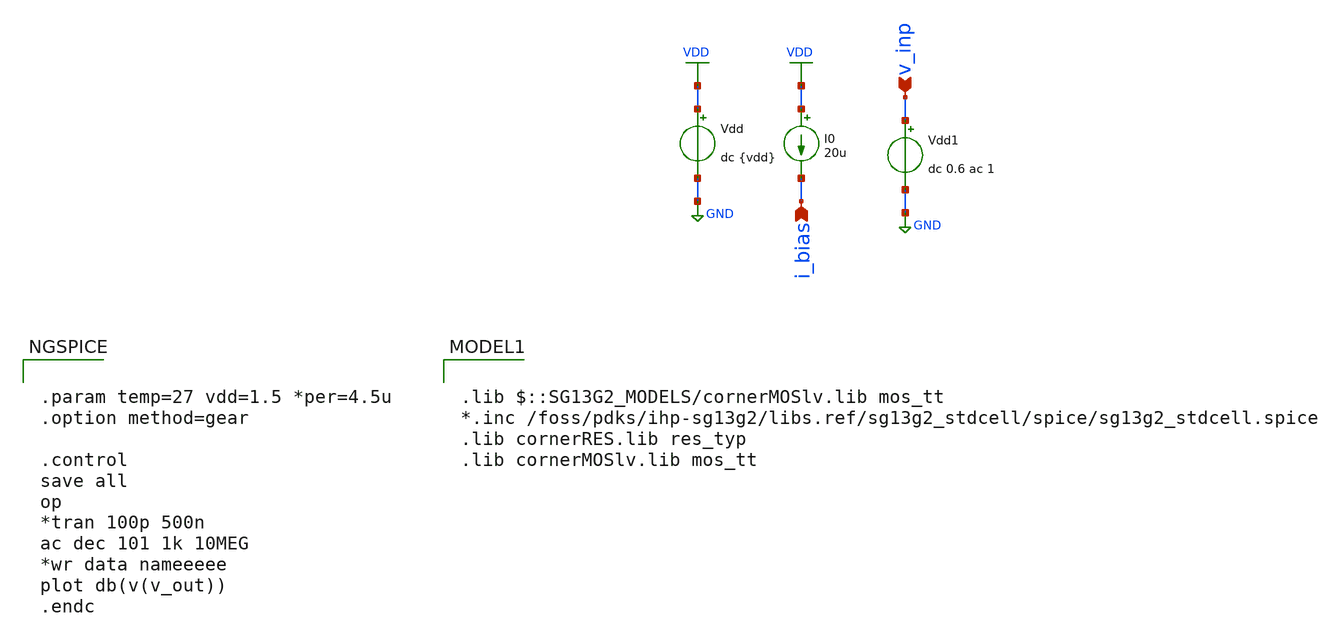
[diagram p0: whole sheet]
** sch_path: 3_Real_Cir/20_Real_Cir/tb_ota.sch
**.subckt tb_ota i_bias v_inp
*.ipin i_bias
*.ipin v_inp
Vdd VDD GND dc {vdd}
I0 VDD i_bias 20u
Vdd1 v_inp GND dc 0.6 ac 1
**** begin user architecture code

.lib $::SG13G2_MODELS/cornerMOSlv.lib mos_tt
*.inc /foss/pdks/ihp-sg13g2/libs.ref/sg13g2_stdcell/spice/sg13g2_stdcell.spice
.lib cornerRES.lib res_typ
.lib cornerMOSlv.lib mos_tt



.param temp=27 vdd=1.5 *per=4.5u
.option method=gear

.control
save all
op
*tran 100p 500n
ac dec 101 1k 10MEG
*wr data nameeeee
plot db(v(v_out))
.endc


**** end user architecture code
**.ends
.GLOBAL GND
.GLOBAL VDD
.end
